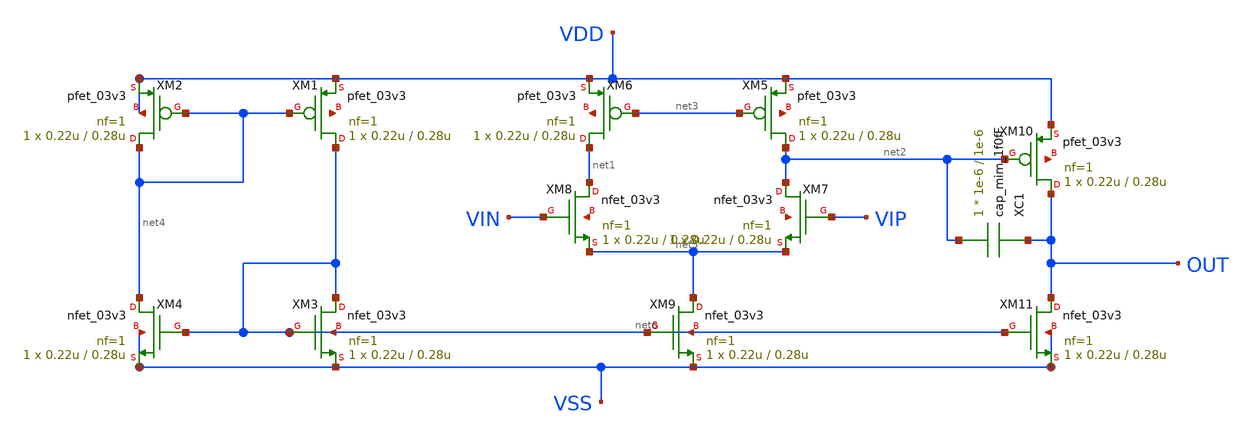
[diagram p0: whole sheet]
** sch_path: week02_current_diffpair/tugas5_cascode_current_mirror/2stageOTA-cascode.sch
**.subckt 2stageOTA-cascode
XM1 net6 net4 VDD net7 pfet_03v3 L=0.28u W=0.22u nf=1 ad='int((nf+1)/2) * W/nf * 0.18u' as='int((nf+2)/2) * W/nf * 0.18u'
+ pd='2*int((nf+1)/2) * (W/nf + 0.18u)' ps='2*int((nf+2)/2) * (W/nf + 0.18u)' nrd='0.18u / W' nrs='0.18u / W'
+ sa=0 sb=0 sd=0 m=1
XM2 net4 net4 VDD VDD pfet_03v3 L=0.28u W=0.22u nf=1 ad='int((nf+1)/2) * W/nf * 0.18u' as='int((nf+2)/2) * W/nf * 0.18u'
+ pd='2*int((nf+1)/2) * (W/nf + 0.18u)' ps='2*int((nf+2)/2) * (W/nf + 0.18u)' nrd='0.18u / W' nrs='0.18u / W'
+ sa=0 sb=0 sd=0 m=1
XM3 net6 net6 VSS net6 nfet_03v3 L=0.28u W=0.22u nf=1 ad='int((nf+1)/2) * W/nf * 0.18u' as='int((nf+2)/2) * W/nf * 0.18u'
+ pd='2*int((nf+1)/2) * (W/nf + 0.18u)' ps='2*int((nf+2)/2) * (W/nf + 0.18u)' nrd='0.18u / W' nrs='0.18u / W'
+ sa=0 sb=0 sd=0 m=1
XM4 net4 net6 VSS VSS nfet_03v3 L=0.28u W=0.22u nf=1 ad='int((nf+1)/2) * W/nf * 0.18u' as='int((nf+2)/2) * W/nf * 0.18u'
+ pd='2*int((nf+1)/2) * (W/nf + 0.18u)' ps='2*int((nf+2)/2) * (W/nf + 0.18u)' nrd='0.18u / W' nrs='0.18u / W'
+ sa=0 sb=0 sd=0 m=1
XM5 net2 net3 VDD net8 pfet_03v3 L=0.28u W=0.22u nf=1 ad='int((nf+1)/2) * W/nf * 0.18u' as='int((nf+2)/2) * W/nf * 0.18u'
+ pd='2*int((nf+1)/2) * (W/nf + 0.18u)' ps='2*int((nf+2)/2) * (W/nf + 0.18u)' nrd='0.18u / W' nrs='0.18u / W'
+ sa=0 sb=0 sd=0 m=1
XM6 net1 net3 VDD net9 pfet_03v3 L=0.28u W=0.22u nf=1 ad='int((nf+1)/2) * W/nf * 0.18u' as='int((nf+2)/2) * W/nf * 0.18u'
+ pd='2*int((nf+1)/2) * (W/nf + 0.18u)' ps='2*int((nf+2)/2) * (W/nf + 0.18u)' nrd='0.18u / W' nrs='0.18u / W'
+ sa=0 sb=0 sd=0 m=1
XM7 net2 VIP net5 net10 nfet_03v3 L=0.28u W=0.22u nf=1 ad='int((nf+1)/2) * W/nf * 0.18u' as='int((nf+2)/2) * W/nf * 0.18u'
+ pd='2*int((nf+1)/2) * (W/nf + 0.18u)' ps='2*int((nf+2)/2) * (W/nf + 0.18u)' nrd='0.18u / W' nrs='0.18u / W'
+ sa=0 sb=0 sd=0 m=1
XM8 net1 VIN net5 net11 nfet_03v3 L=0.28u W=0.22u nf=1 ad='int((nf+1)/2) * W/nf * 0.18u' as='int((nf+2)/2) * W/nf * 0.18u'
+ pd='2*int((nf+1)/2) * (W/nf + 0.18u)' ps='2*int((nf+2)/2) * (W/nf + 0.18u)' nrd='0.18u / W' nrs='0.18u / W'
+ sa=0 sb=0 sd=0 m=1
XM9 net5 net6 VSS net6 nfet_03v3 L=0.28u W=0.22u nf=1 ad='int((nf+1)/2) * W/nf * 0.18u' as='int((nf+2)/2) * W/nf * 0.18u'
+ pd='2*int((nf+1)/2) * (W/nf + 0.18u)' ps='2*int((nf+2)/2) * (W/nf + 0.18u)' nrd='0.18u / W' nrs='0.18u / W'
+ sa=0 sb=0 sd=0 m=1
XM10 OUT net2 VDD net12 pfet_03v3 L=0.28u W=0.22u nf=1 ad='int((nf+1)/2) * W/nf * 0.18u' as='int((nf+2)/2) * W/nf * 0.18u'
+ pd='2*int((nf+1)/2) * (W/nf + 0.18u)' ps='2*int((nf+2)/2) * (W/nf + 0.18u)' nrd='0.18u / W' nrs='0.18u / W'
+ sa=0 sb=0 sd=0 m=1
XM11 OUT net6 VSS VSS nfet_03v3 L=0.28u W=0.22u nf=1 ad='int((nf+1)/2) * W/nf * 0.18u' as='int((nf+2)/2) * W/nf * 0.18u'
+ pd='2*int((nf+1)/2) * (W/nf + 0.18u)' ps='2*int((nf+2)/2) * (W/nf + 0.18u)' nrd='0.18u / W' nrs='0.18u / W'
+ sa=0 sb=0 sd=0 m=1
XC1 OUT net2 cap_mim_1f0fF c_width=1e-6 c_length=1e-6 m=1
**.ends
.end
